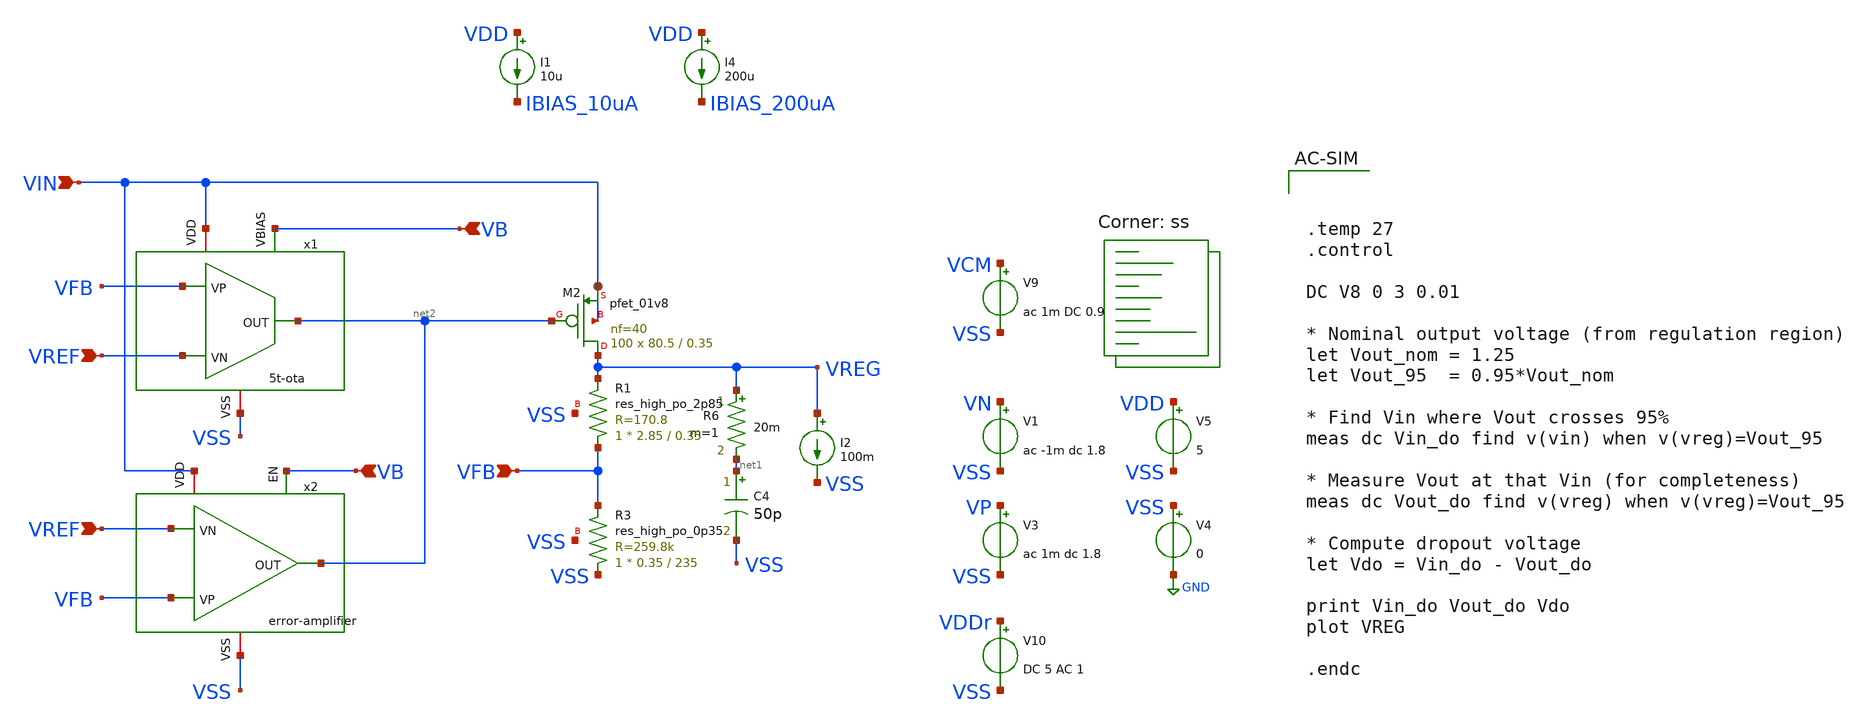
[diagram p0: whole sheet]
** sch_path: xschem/ldo-core/schematics/ldo-core.sch
**.subckt ldo-core VIN VB VREF VB VREF VFB
*.ipin VIN
*.ipin VB
*.ipin VREF
*.ipin VB
*.ipin VREF
*.ipin VFB
XM2 VREG net2 VIN VIN sky130_fd_pr__pfet_01v8 L=0.35 W=80.5 nf=40 ad='int((nf+1)/2) * W/nf * 0.29' as='int((nf+2)/2) * W/nf * 0.29'
+ pd='2*int((nf+1)/2) * (W/nf + 0.29)' ps='2*int((nf+2)/2) * (W/nf + 0.29)' nrd='0.29 / W' nrs='0.29 / W'
+ sa=0 sb=0 sd=0 mult=100 m=100
I2 VREG VSS 100m
C4 net1 VSS 50p m=1
R6 VREG net1 20m m=1
XR3 VSS VFB VSS sky130_fd_pr__res_high_po_0p35 L=235 mult=1 m=1
XR1 VFB VREG VSS sky130_fd_pr__res_high_po_2p85 L=0.35 mult=1 m=1
x1 VIN net2 VFB VREF VB VSS 5t-ota
x2 VIN net2 VFB VREF VB VSS error-amplifier
V1 VN VSS ac -1m dc 1.8
V3 VP VSS ac 1m dc 1.8
V5 VDD VSS 5
V4 VSS GND 0
I4 VDD IBIAS_200uA 200u
V9 VCM VSS ac 1m DC 0.9
V10 VDDr VSS DC 5 AC 1
I1 VDD IBIAS_10uA 10u
**** begin user architecture code



.temp 27
.control

DC V8 0 3 0.01

* Nominal output voltage (from regulation region)
let Vout_nom = 1.25
let Vout_95  = 0.95*Vout_nom

* Find Vin where Vout crosses 95%
meas dc Vin_do find v(vin) when v(vreg)=Vout_95

* Measure Vout at that Vin (for completeness)
meas dc Vout_do find v(vreg) when v(vreg)=Vout_95

* Compute dropout voltage
let Vdo = Vin_do - Vout_do

print Vin_do Vout_do Vdo
plot VREG

.endc


.lib $::SKYWATER_MODELS/sky130.lib.spice ss
**** end user architecture code
**.ends
.GLOBAL GND
.end
